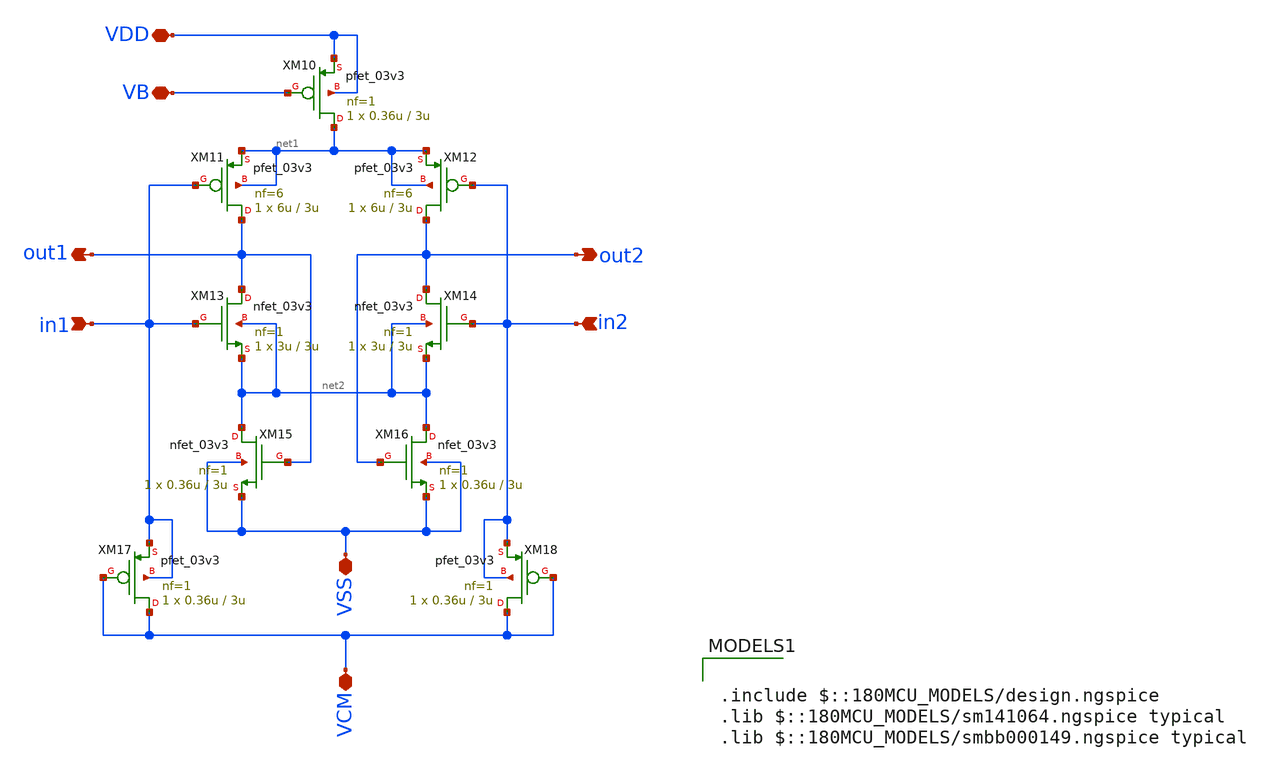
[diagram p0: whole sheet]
** sch_path: ISSCC26/submitted_notebooks/Low Mismatch 4 Channels Instrumentation Amplifier/Instrumentation Amplifier/Schematic and Testbench/INA_STAGE_FIXED.sch
**.subckt INA_STAGE_FIXED out1 out2 in1 in2 VDD VB VSS VCM
*.opin out1
*.opin out2
*.ipin in1
*.ipin in2
*.iopin VDD
*.iopin VB
*.iopin VSS
*.iopin VCM
XM10 net1 VB VDD VDD pfet_03v3 L=3u W=0.36u nf=1 ad='int((nf+1)/2) * W/nf * 0.18u' as='int((nf+2)/2) * W/nf * 0.18u'
+ pd='2*int((nf+1)/2) * (W/nf + 0.18u)' ps='2*int((nf+2)/2) * (W/nf + 0.18u)' nrd='0.18u / W' nrs='0.18u / W'
+ sa=0 sb=0 sd=0 m=1
XM11 out1 in1 net1 net1 pfet_03v3 L=3u W=6u nf=6 ad='int((nf+1)/2) * W/nf * 0.18u' as='int((nf+2)/2) * W/nf * 0.18u'
+ pd='2*int((nf+1)/2) * (W/nf + 0.18u)' ps='2*int((nf+2)/2) * (W/nf + 0.18u)' nrd='0.18u / W' nrs='0.18u / W'
+ sa=0 sb=0 sd=0 m=1
XM12 out2 in2 net1 net1 pfet_03v3 L=3u W=6u nf=6 ad='int((nf+1)/2) * W/nf * 0.18u' as='int((nf+2)/2) * W/nf * 0.18u'
+ pd='2*int((nf+1)/2) * (W/nf + 0.18u)' ps='2*int((nf+2)/2) * (W/nf + 0.18u)' nrd='0.18u / W' nrs='0.18u / W'
+ sa=0 sb=0 sd=0 m=1
XM13 out1 in1 net2 net2 nfet_03v3 L=3u W=3u nf=1 ad='int((nf+1)/2) * W/nf * 0.18u' as='int((nf+2)/2) * W/nf * 0.18u'
+ pd='2*int((nf+1)/2) * (W/nf + 0.18u)' ps='2*int((nf+2)/2) * (W/nf + 0.18u)' nrd='0.18u / W' nrs='0.18u / W'
+ sa=0 sb=0 sd=0 m=1
XM14 out2 in2 net2 net2 nfet_03v3 L=3u W=3u nf=1 ad='int((nf+1)/2) * W/nf * 0.18u' as='int((nf+2)/2) * W/nf * 0.18u'
+ pd='2*int((nf+1)/2) * (W/nf + 0.18u)' ps='2*int((nf+2)/2) * (W/nf + 0.18u)' nrd='0.18u / W' nrs='0.18u / W'
+ sa=0 sb=0 sd=0 m=1
XM15 net2 out1 VSS VSS nfet_03v3 L=3u W=0.36u nf=1 ad='int((nf+1)/2) * W/nf * 0.18u' as='int((nf+2)/2) * W/nf * 0.18u'
+ pd='2*int((nf+1)/2) * (W/nf + 0.18u)' ps='2*int((nf+2)/2) * (W/nf + 0.18u)' nrd='0.18u / W' nrs='0.18u / W'
+ sa=0 sb=0 sd=0 m=1
XM16 net2 out2 VSS VSS nfet_03v3 L=3u W=0.36u nf=1 ad='int((nf+1)/2) * W/nf * 0.18u' as='int((nf+2)/2) * W/nf * 0.18u'
+ pd='2*int((nf+1)/2) * (W/nf + 0.18u)' ps='2*int((nf+2)/2) * (W/nf + 0.18u)' nrd='0.18u / W' nrs='0.18u / W'
+ sa=0 sb=0 sd=0 m=1
XM17 VCM VCM in1 in1 pfet_03v3 L=3u W=0.36u nf=1 ad='int((nf+1)/2) * W/nf * 0.18u' as='int((nf+2)/2) * W/nf * 0.18u'
+ pd='2*int((nf+1)/2) * (W/nf + 0.18u)' ps='2*int((nf+2)/2) * (W/nf + 0.18u)' nrd='0.18u / W' nrs='0.18u / W'
+ sa=0 sb=0 sd=0 m=1
XM18 VCM VCM in2 in2 pfet_03v3 L=3u W=0.36u nf=1 ad='int((nf+1)/2) * W/nf * 0.18u' as='int((nf+2)/2) * W/nf * 0.18u'
+ pd='2*int((nf+1)/2) * (W/nf + 0.18u)' ps='2*int((nf+2)/2) * (W/nf + 0.18u)' nrd='0.18u / W' nrs='0.18u / W'
+ sa=0 sb=0 sd=0 m=1
**** begin user architecture code

.include $::180MCU_MODELS/design.ngspice
.lib $::180MCU_MODELS/sm141064.ngspice typical
.lib $::180MCU_MODELS/smbb000149.ngspice typical

**** end user architecture code
**.ends
.end
